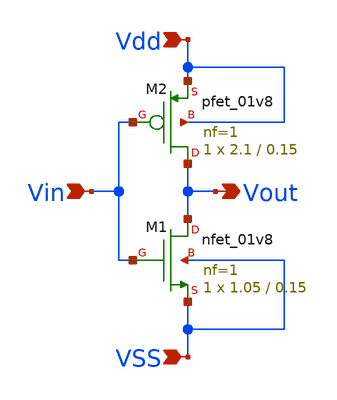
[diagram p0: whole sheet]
** sch_path: trabajosPracticos/tp6/archivosXschem/41schematicDesignActividad2.sch
**.subckt 41schematicDesignActividad2 Vdd Vin VSS Vout
*.ipin Vdd
*.ipin Vin
*.ipin VSS
*.opin Vout
XM1 Vout Vin VSS VSS sky130_fd_pr__nfet_01v8 L=0.15 W=1.05 nf=1 ad='int((nf+1)/2) * W/nf * 0.29' as='int((nf+2)/2) * W/nf * 0.29'
+ pd='2*int((nf+1)/2) * (W/nf + 0.29)' ps='2*int((nf+2)/2) * (W/nf + 0.29)' nrd='0.29 / W' nrs='0.29 / W'
+ sa=0 sb=0 sd=0 mult=1 m=1
XM2 Vout Vin Vdd Vdd sky130_fd_pr__pfet_01v8 L=0.15 W=2.1 nf=1 ad='int((nf+1)/2) * W/nf * 0.29' as='int((nf+2)/2) * W/nf * 0.29'
+ pd='2*int((nf+1)/2) * (W/nf + 0.29)' ps='2*int((nf+2)/2) * (W/nf + 0.29)' nrd='0.29 / W' nrs='0.29 / W'
+ sa=0 sb=0 sd=0 mult=1 m=1
**.ends
.end
